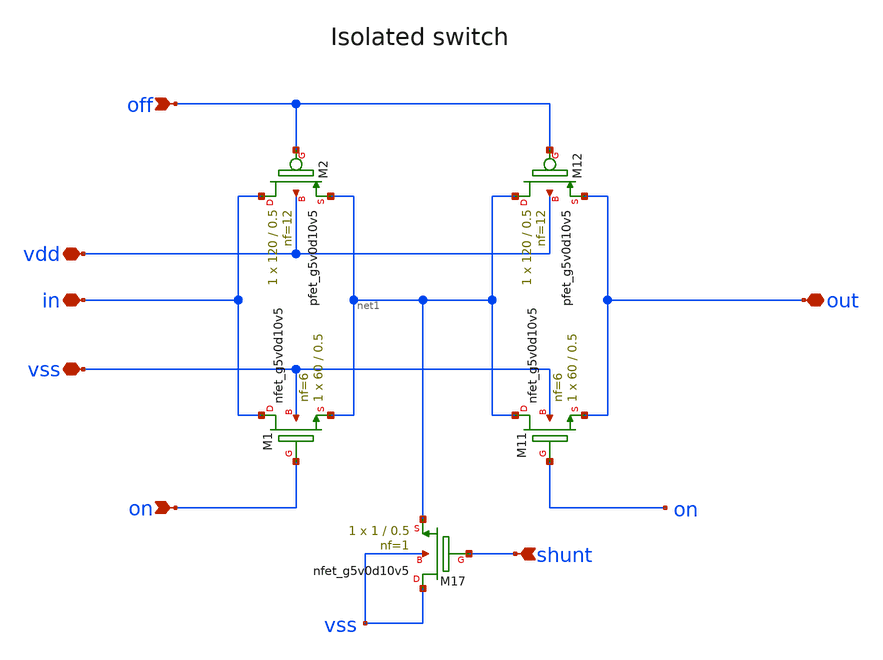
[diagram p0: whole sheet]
** sch_path: analog/repairs/adc_repaired/ip/sky130_ef_ip__cdac3v_12bit/dependencies/sky130_ef_ip__analog_switches/xschem/isolated_switch_4.sch
**.subckt isolated_switch_4 on out vdd vss in off shunt
*.ipin on
*.iopin out
*.iopin vdd
*.iopin vss
*.iopin in
*.ipin off
*.ipin shunt
XM1 in on net1 vss sky130_fd_pr__nfet_g5v0d10v5 L=0.5 W=60 nf=6 ad='int((nf+1)/2) * W/nf * 0.29' as='int((nf+2)/2) * W/nf * 0.29'
+ pd='2*int((nf+1)/2) * (W/nf + 0.29)' ps='2*int((nf+2)/2) * (W/nf + 0.29)' nrd='0.29 / W' nrs='0.29 / W'
+ sa=0 sb=0 sd=0 mult=1 m=1
XM2 in off net1 vdd sky130_fd_pr__pfet_g5v0d10v5 L=0.5 W=120 nf=12 ad='int((nf+1)/2) * W/nf * 0.29' as='int((nf+2)/2) * W/nf * 0.29'
+ pd='2*int((nf+1)/2) * (W/nf + 0.29)' ps='2*int((nf+2)/2) * (W/nf + 0.29)' nrd='0.29 / W' nrs='0.29 / W'
+ sa=0 sb=0 sd=0 mult=1 m=1
XM11 net1 on out vss sky130_fd_pr__nfet_g5v0d10v5 L=0.5 W=60 nf=6 ad='int((nf+1)/2) * W/nf * 0.29' as='int((nf+2)/2) * W/nf * 0.29'
+ pd='2*int((nf+1)/2) * (W/nf + 0.29)' ps='2*int((nf+2)/2) * (W/nf + 0.29)' nrd='0.29 / W' nrs='0.29 / W'
+ sa=0 sb=0 sd=0 mult=1 m=1
XM12 net1 off out vdd sky130_fd_pr__pfet_g5v0d10v5 L=0.5 W=120 nf=12 ad='int((nf+1)/2) * W/nf * 0.29'
+ as='int((nf+2)/2) * W/nf * 0.29' pd='2*int((nf+1)/2) * (W/nf + 0.29)' ps='2*int((nf+2)/2) * (W/nf + 0.29)'
+ nrd='0.29 / W' nrs='0.29 / W' sa=0 sb=0 sd=0 mult=1 m=1
XM17 vss shunt net1 vss sky130_fd_pr__nfet_g5v0d10v5 L=0.5 W=1 nf=1 ad='int((nf+1)/2) * W/nf * 0.29'
+ as='int((nf+2)/2) * W/nf * 0.29' pd='2*int((nf+1)/2) * (W/nf + 0.29)' ps='2*int((nf+2)/2) * (W/nf + 0.29)'
+ nrd='0.29 / W' nrs='0.29 / W' sa=0 sb=0 sd=0 mult=1 m=1
**.ends
.end
